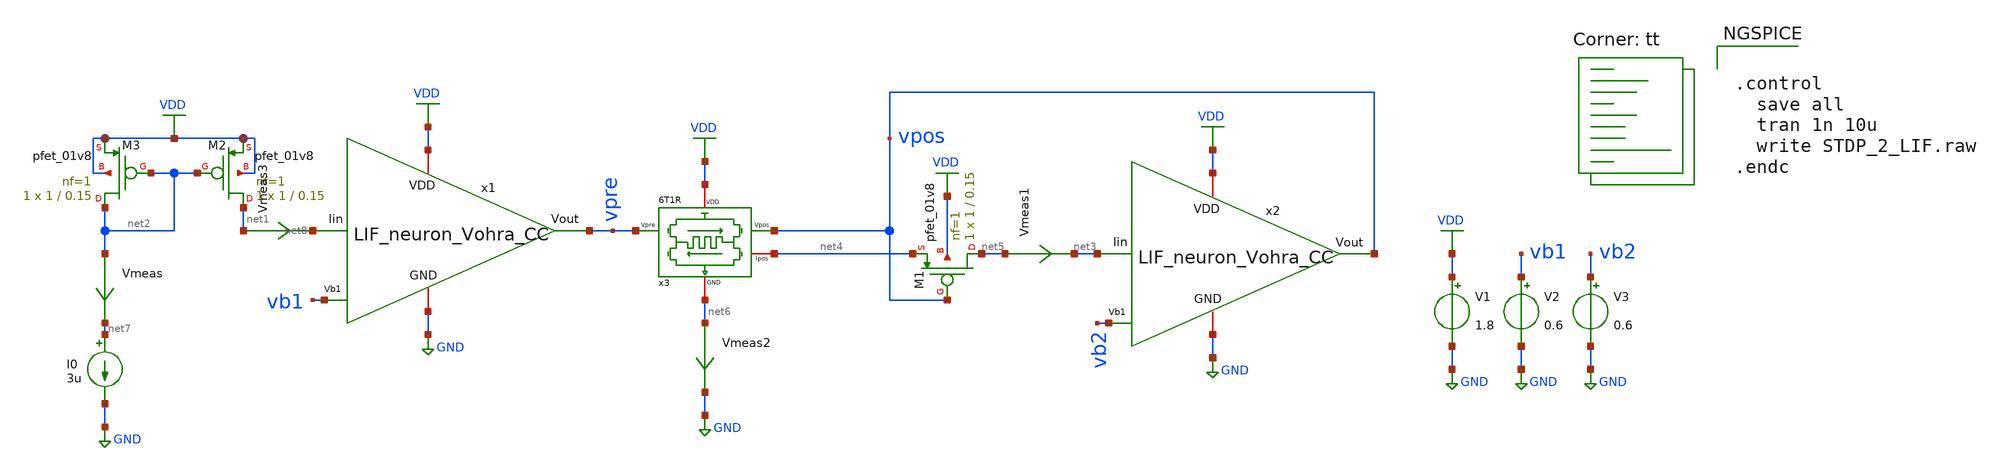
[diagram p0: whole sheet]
** sch_path: STDP/STDP_2_LIF_6T1R_dc.sch
**.subckt STDP_2_LIF_6T1R_dc
V1 VDD GND 1.8
V2 vb1 GND 0.6
x3 VDD net4 vpre vpos net6 6T1R
x1 VDD vpre vb1 GND net8 LIF_neuron_Vohra_CC
I0 net7 GND 3u
XM2 net1 net2 VDD VDD sky130_fd_pr__pfet_01v8 L=0.15 W=1 nf=1 ad='int((nf+1)/2) * W/nf * 0.29' as='int((nf+2)/2) * W/nf * 0.29'
+ pd='2*int((nf+1)/2) * (W/nf + 0.29)' ps='2*int((nf+2)/2) * (W/nf + 0.29)' nrd='0.29 / W' nrs='0.29 / W'
+ sa=0 sb=0 sd=0 mult=1 m=1
XM3 net2 net2 VDD VDD sky130_fd_pr__pfet_01v8 L=0.15 W=1 nf=1 ad='int((nf+1)/2) * W/nf * 0.29' as='int((nf+2)/2) * W/nf * 0.29'
+ pd='2*int((nf+1)/2) * (W/nf + 0.29)' ps='2*int((nf+2)/2) * (W/nf + 0.29)' nrd='0.29 / W' nrs='0.29 / W'
+ sa=0 sb=0 sd=0 mult=1 m=1
x2 VDD vpos vb2 GND net3 LIF_neuron_Vohra_CC
XM1 net5 vpos net4 VDD sky130_fd_pr__pfet_01v8 L=0.15 W=1 nf=1 ad='int((nf+1)/2) * W/nf * 0.29' as='int((nf+2)/2) * W/nf * 0.29'
+ pd='2*int((nf+1)/2) * (W/nf + 0.29)' ps='2*int((nf+2)/2) * (W/nf + 0.29)' nrd='0.29 / W' nrs='0.29 / W'
+ sa=0 sb=0 sd=0 mult=1 m=1
Vmeas1 net5 net3 0
.save i(vmeas1)
V3 vb2 GND 0.6
Vmeas2 net6 GND 0
.save i(vmeas2)
Vmeas net2 net7 0
.save i(vmeas)
Vmeas3 net1 net8 0
.save i(vmeas3)
**** begin user architecture code
.lib $::SKYWATER_MODELS/sky130.lib.spice tt

** opencircuitdesign pdks install
.inc $::SKYWATER_MODELS/rram_v0.spice



.control
  save all
  tran 1n 10u
  write STDP_2_LIF.raw
.endc


**** end user architecture code
**.ends

* expanding   symbol:  /home/ricardo/RATT_repos/Proyectos_xschem/synapse/6T1R.sym # of pins=5
** sym_path: synapse/6T1R.sym
** sch_path: synapse/6T1R.sch
.subckt 6T1R VDD Ipos Vpre Vpos GND
*.ipin Vpre
*.ipin Vpos
*.iopin GND
*.iopin Ipos
*.iopin VDD
XM1 vipre Vpre net1 GND sky130_fd_pr__nfet_01v8 L=0.15 W=10 nf=1 ad='int((nf+1)/2) * W/nf * 0.29' as='int((nf+2)/2) * W/nf * 0.29'
+ pd='2*int((nf+1)/2) * (W/nf + 0.29)' ps='2*int((nf+2)/2) * (W/nf + 0.29)' nrd='0.29 / W' nrs='0.29 / W'
+ sa=0 sb=0 sd=0 mult=1 m=1
XR1 net2 net1 rram_v0
XM3 vipre Vpos net2 GND sky130_fd_pr__nfet_01v8 L=0.15 W=1 nf=1 ad='int((nf+1)/2) * W/nf * 0.29' as='int((nf+2)/2) * W/nf * 0.29'
+ pd='2*int((nf+1)/2) * (W/nf + 0.29)' ps='2*int((nf+2)/2) * (W/nf + 0.29)' nrd='0.29 / W' nrs='0.29 / W'
+ sa=0 sb=0 sd=0 mult=1 m=1
XM6 Ipos vipre VDD VDD sky130_fd_pr__pfet_01v8 L=0.15 W=1 nf=1 ad='int((nf+1)/2) * W/nf * 0.29' as='int((nf+2)/2) * W/nf * 0.29'
+ pd='2*int((nf+1)/2) * (W/nf + 0.29)' ps='2*int((nf+2)/2) * (W/nf + 0.29)' nrd='0.29 / W' nrs='0.29 / W'
+ sa=0 sb=0 sd=0 mult=1 m=1
XM5 vipre vipre VDD VDD sky130_fd_pr__pfet_01v8 L=0.15 W=20 nf=1 ad='int((nf+1)/2) * W/nf * 0.29' as='int((nf+2)/2) * W/nf * 0.29'
+ pd='2*int((nf+1)/2) * (W/nf + 0.29)' ps='2*int((nf+2)/2) * (W/nf + 0.29)' nrd='0.29 / W' nrs='0.29 / W'
+ sa=0 sb=0 sd=0 mult=1 m=1
XM2 net1 Vpos GND GND sky130_fd_pr__nfet_01v8 L=0.15 W=1 nf=1 ad='int((nf+1)/2) * W/nf * 0.29' as='int((nf+2)/2) * W/nf * 0.29'
+ pd='2*int((nf+1)/2) * (W/nf + 0.29)' ps='2*int((nf+2)/2) * (W/nf + 0.29)' nrd='0.29 / W' nrs='0.29 / W'
+ sa=0 sb=0 sd=0 mult=1 m=1
XM4 net2 Vpre GND GND sky130_fd_pr__nfet_01v8 L=0.15 W=10 nf=1 ad='int((nf+1)/2) * W/nf * 0.29' as='int((nf+2)/2) * W/nf * 0.29'
+ pd='2*int((nf+1)/2) * (W/nf + 0.29)' ps='2*int((nf+2)/2) * (W/nf + 0.29)' nrd='0.29 / W' nrs='0.29 / W'
+ sa=0 sb=0 sd=0 mult=1 m=1
.ends


* expanding   symbol:  /home/ricardo/RATT_repos/Proyectos_xschem/LIF_neuron/LIF_neuron_Vohra_CC.sym
*+ # of pins=5
** sym_path: LIF_neuron/LIF_neuron_Vohra_CC.sym
** sch_path: LIF_neuron/LIF_neuron_Vohra_CC.sch
.subckt LIF_neuron_Vohra_CC VDD Vout Vb1 GND Iin
*.iopin GND
*.ipin Vb1
*.iopin VDD
*.opin Vout
*.ipin Iin
XM8 net2 Vb1 GND GND sky130_fd_pr__nfet_01v8 L=0.5 W=5 nf=1 ad='int((nf+1)/2) * W/nf * 0.29' as='int((nf+2)/2) * W/nf * 0.29'
+ pd='2*int((nf+1)/2) * (W/nf + 0.29)' ps='2*int((nf+2)/2) * (W/nf + 0.29)' nrd='0.29 / W' nrs='0.29 / W'
+ sa=0 sb=0 sd=0 mult=1 m=1
XM7 rc net1 net2 GND sky130_fd_pr__nfet_01v8 L=1 W=1 nf=1 ad='int((nf+1)/2) * W/nf * 0.29' as='int((nf+2)/2) * W/nf * 0.29'
+ pd='2*int((nf+1)/2) * (W/nf + 0.29)' ps='2*int((nf+2)/2) * (W/nf + 0.29)' nrd='0.29 / W' nrs='0.29 / W'
+ sa=0 sb=0 sd=0 mult=1 m=1
XM6 rc net1 VDD VDD sky130_fd_pr__pfet_01v8 L=1 W=5 nf=1 ad='int((nf+1)/2) * W/nf * 0.29' as='int((nf+2)/2) * W/nf * 0.29'
+ pd='2*int((nf+1)/2) * (W/nf + 0.29)' ps='2*int((nf+2)/2) * (W/nf + 0.29)' nrd='0.29 / W' nrs='0.29 / W'
+ sa=0 sb=0 sd=0 mult=1 m=1
XCr rc GND sky130_fd_pr__cap_mim_m3_1 W=10 L=1 MF=1 m=1
XM9 Iin rc GND GND sky130_fd_pr__nfet_01v8 L=1 W=5 nf=1 ad='int((nf+1)/2) * W/nf * 0.29' as='int((nf+2)/2) * W/nf * 0.29'
+ pd='2*int((nf+1)/2) * (W/nf + 0.29)' ps='2*int((nf+2)/2) * (W/nf + 0.29)' nrd='0.29 / W' nrs='0.29 / W'
+ sa=0 sb=0 sd=0 mult=1 m=1
XCm Iin GND sky130_fd_pr__cap_mim_m3_1 W=30 L=1 MF=50 m=50
XM5 net3 Vout GND GND sky130_fd_pr__nfet_01v8 L=0.5 W=1 nf=1 ad='int((nf+1)/2) * W/nf * 0.29' as='int((nf+2)/2) * W/nf * 0.29'
+ pd='2*int((nf+1)/2) * (W/nf + 0.29)' ps='2*int((nf+2)/2) * (W/nf + 0.29)' nrd='0.29 / W' nrs='0.29 / W'
+ sa=0 sb=0 sd=0 mult=1 m=1
XM3 net1 Iin net3 GND sky130_fd_pr__nfet_01v8 L=1 W=1 nf=1 ad='int((nf+1)/2) * W/nf * 0.29' as='int((nf+2)/2) * W/nf * 0.29'
+ pd='2*int((nf+1)/2) * (W/nf + 0.29)' ps='2*int((nf+2)/2) * (W/nf + 0.29)' nrd='0.29 / W' nrs='0.29 / W'
+ sa=0 sb=0 sd=0 mult=1 m=1
XM1 net1 Iin VDD VDD sky130_fd_pr__pfet_01v8 L=1 W=1 nf=1 ad='int((nf+1)/2) * W/nf * 0.29' as='int((nf+2)/2) * W/nf * 0.29'
+ pd='2*int((nf+1)/2) * (W/nf + 0.29)' ps='2*int((nf+2)/2) * (W/nf + 0.29)' nrd='0.29 / W' nrs='0.29 / W'
+ sa=0 sb=0 sd=0 mult=1 m=1
XM4 Vout net1 net3 GND sky130_fd_pr__nfet_01v8 L=1 W=1 nf=1 ad='int((nf+1)/2) * W/nf * 0.29' as='int((nf+2)/2) * W/nf * 0.29'
+ pd='2*int((nf+1)/2) * (W/nf + 0.29)' ps='2*int((nf+2)/2) * (W/nf + 0.29)' nrd='0.29 / W' nrs='0.29 / W'
+ sa=0 sb=0 sd=0 mult=1 m=1
XM2 Vout net1 VDD VDD sky130_fd_pr__pfet_01v8 L=1 W=5 nf=1 ad='int((nf+1)/2) * W/nf * 0.29' as='int((nf+2)/2) * W/nf * 0.29'
+ pd='2*int((nf+1)/2) * (W/nf + 0.29)' ps='2*int((nf+2)/2) * (W/nf + 0.29)' nrd='0.29 / W' nrs='0.29 / W'
+ sa=0 sb=0 sd=0 mult=1 m=1
.ends

.GLOBAL GND
.GLOBAL VDD
.end
